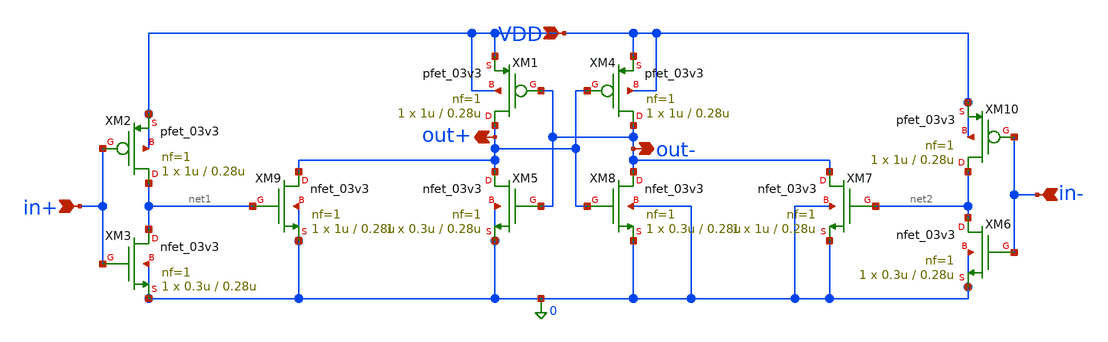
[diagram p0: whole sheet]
** sch_path: Design_Files/IC Design/Schematic/SAR_ADC_BLOCKS/RS_LATCH/RS_LATCH.sch
**.subckt RS_LATCH VDD in+ in- out+ out-
*.ipin VDD
*.ipin in+
*.ipin in-
*.opin out+
*.opin out-
XM4 out- out+ VDD VDD pfet_03v3 L=0.28u W=1u nf=1 ad='int((nf+1)/2) * W/nf * 0.18u' as='int((nf+2)/2) * W/nf * 0.18u'
+ pd='2*int((nf+1)/2) * (W/nf + 0.18u)' ps='2*int((nf+2)/2) * (W/nf + 0.18u)' nrd='0.18u / W' nrs='0.18u / W'
+ sa=0 sb=0 sd=0 m=1
XM8 out- out+ 0 0 nfet_03v3 L=0.28u W=0.3u nf=1 ad='int((nf+1)/2) * W/nf * 0.18u' as='int((nf+2)/2) * W/nf * 0.18u'
+ pd='2*int((nf+1)/2) * (W/nf + 0.18u)' ps='2*int((nf+2)/2) * (W/nf + 0.18u)' nrd='0.18u / W' nrs='0.18u / W'
+ sa=0 sb=0 sd=0 m=1
XM9 out+ net1 0 0 nfet_03v3 L=0.28u W=1u nf=1 ad='int((nf+1)/2) * W/nf * 0.18u' as='int((nf+2)/2) * W/nf * 0.18u'
+ pd='2*int((nf+1)/2) * (W/nf + 0.18u)' ps='2*int((nf+2)/2) * (W/nf + 0.18u)' nrd='0.18u / W' nrs='0.18u / W'
+ sa=0 sb=0 sd=0 m=1
XM5 out+ out- 0 0 nfet_03v3 L=0.28u W=0.3u nf=1 ad='int((nf+1)/2) * W/nf * 0.18u' as='int((nf+2)/2) * W/nf * 0.18u'
+ pd='2*int((nf+1)/2) * (W/nf + 0.18u)' ps='2*int((nf+2)/2) * (W/nf + 0.18u)' nrd='0.18u / W' nrs='0.18u / W'
+ sa=0 sb=0 sd=0 m=1
XM7 out- net2 0 0 nfet_03v3 L=0.28u W=1u nf=1 ad='int((nf+1)/2) * W/nf * 0.18u' as='int((nf+2)/2) * W/nf * 0.18u'
+ pd='2*int((nf+1)/2) * (W/nf + 0.18u)' ps='2*int((nf+2)/2) * (W/nf + 0.18u)' nrd='0.18u / W' nrs='0.18u / W'
+ sa=0 sb=0 sd=0 m=1
XM1 out+ out- VDD VDD pfet_03v3 L=0.28u W=1u nf=1 ad='int((nf+1)/2) * W/nf * 0.18u' as='int((nf+2)/2) * W/nf * 0.18u'
+ pd='2*int((nf+1)/2) * (W/nf + 0.18u)' ps='2*int((nf+2)/2) * (W/nf + 0.18u)' nrd='0.18u / W' nrs='0.18u / W'
+ sa=0 sb=0 sd=0 m=1
XM2 net1 in+ VDD VDD pfet_03v3 L=0.28u W=1u nf=1 ad='int((nf+1)/2) * W/nf * 0.18u' as='int((nf+2)/2) * W/nf * 0.18u'
+ pd='2*int((nf+1)/2) * (W/nf + 0.18u)' ps='2*int((nf+2)/2) * (W/nf + 0.18u)' nrd='0.18u / W' nrs='0.18u / W'
+ sa=0 sb=0 sd=0 m=1
XM3 net1 in+ 0 0 nfet_03v3 L=0.28u W=0.3u nf=1 ad='int((nf+1)/2) * W/nf * 0.18u' as='int((nf+2)/2) * W/nf * 0.18u'
+ pd='2*int((nf+1)/2) * (W/nf + 0.18u)' ps='2*int((nf+2)/2) * (W/nf + 0.18u)' nrd='0.18u / W' nrs='0.18u / W'
+ sa=0 sb=0 sd=0 m=1
XM6 net2 in- 0 0 nfet_03v3 L=0.28u W=0.3u nf=1 ad='int((nf+1)/2) * W/nf * 0.18u' as='int((nf+2)/2) * W/nf * 0.18u'
+ pd='2*int((nf+1)/2) * (W/nf + 0.18u)' ps='2*int((nf+2)/2) * (W/nf + 0.18u)' nrd='0.18u / W' nrs='0.18u / W'
+ sa=0 sb=0 sd=0 m=1
XM10 net2 in- VDD VDD pfet_03v3 L=0.28u W=1u nf=1 ad='int((nf+1)/2) * W/nf * 0.18u' as='int((nf+2)/2) * W/nf * 0.18u'
+ pd='2*int((nf+1)/2) * (W/nf + 0.18u)' ps='2*int((nf+2)/2) * (W/nf + 0.18u)' nrd='0.18u / W' nrs='0.18u / W'
+ sa=0 sb=0 sd=0 m=1
**.ends
.end
